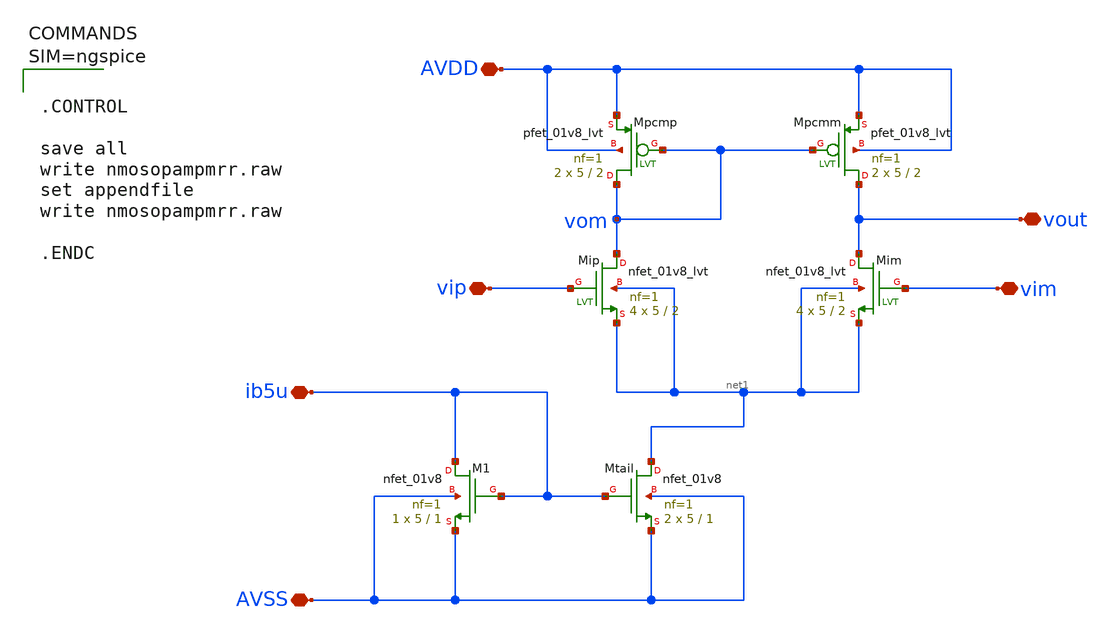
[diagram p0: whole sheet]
** sch_path: work/xschem/nmosopampmrr.sch
**.subckt nmosopampmrr ib5u vip vim AVDD AVSS vout
*.iopin ib5u
*.iopin vip
*.iopin vim
*.iopin AVDD
*.iopin AVSS
*.iopin vout
XMtail net1 ib5u AVSS AVSS sky130_fd_pr__nfet_01v8 L=1 W=5 nf=1 ad='int((1 + 1)/2) * 5 / 1 * 0.29' as='int((1 + 2)/2) * 5 / 1 * 0.29'
+ pd='2*int((1 + 1)/2) * (5 / 1 + 0.29)' ps='2*int((1 + 2)/2) * (5 / 1 + 0.29)' nrd='0.29 / 5 ' nrs='0.29 / 5 '
+ sa=0 sb=0 sd=0 mult=2 m=2
XM1 ib5u ib5u AVSS AVSS sky130_fd_pr__nfet_01v8 L=1 W=5 nf=1 ad='int((1 + 1)/2) * 5 / 1 * 0.29' as='int((1 + 2)/2) * 5 / 1 * 0.29'
+ pd='2*int((1 + 1)/2) * (5 / 1 + 0.29)' ps='2*int((1 + 2)/2) * (5 / 1 + 0.29)' nrd='0.29 / 5 ' nrs='0.29 / 5 '
+ sa=0 sb=0 sd=0 mult=1 m=1
XMip vom vip net1 net1 sky130_fd_pr__nfet_01v8_lvt L=2 W=5 nf=1 ad='int((1 + 1)/2) * 5 / 1 * 0.29' as='int((1 + 2)/2) * 5 / 1 * 0.29'
+ pd='2*int((1 + 1)/2) * (5 / 1 + 0.29)' ps='2*int((1 + 2)/2) * (5 / 1 + 0.29)' nrd='0.29 / 5 ' nrs='0.29 / 5 '
+ sa=0 sb=0 sd=0 mult=4 m=4
XMim vout vim net1 net1 sky130_fd_pr__nfet_01v8_lvt L=2 W=5 nf=1 ad='int((1 + 1)/2) * 5 / 1 * 0.29' as='int((1 + 2)/2) * 5 / 1 * 0.29'
+ pd='2*int((1 + 1)/2) * (5 / 1 + 0.29)' ps='2*int((1 + 2)/2) * (5 / 1 + 0.29)' nrd='0.29 / 5 ' nrs='0.29 / 5 '
+ sa=0 sb=0 sd=0 mult=4 m=4
XMpcmm vout vom AVDD AVDD sky130_fd_pr__pfet_01v8_lvt L=2 W=5 nf=1 ad='int((1 + 1)/2) * 5 / 1 * 0.29'
+ as='int((1 + 2)/2) * 5 / 1 * 0.29' pd='2*int((1 + 1)/2) * (5 / 1 + 0.29)' ps='2*int((1 + 2)/2) * (5 / 1 + 0.29)'
+ nrd='0.29 / 5 ' nrs='0.29 / 5 ' sa=0 sb=0 sd=0 mult=2 m=2
XMpcmp vom vom AVDD AVDD sky130_fd_pr__pfet_01v8_lvt L=2 W=5 nf=1 ad='int((1 + 1)/2) * 5 / 1 * 0.29'
+ as='int((1 + 2)/2) * 5 / 1 * 0.29' pd='2*int((1 + 1)/2) * (5 / 1 + 0.29)' ps='2*int((1 + 2)/2) * (5 / 1 + 0.29)'
+ nrd='0.29 / 5 ' nrs='0.29 / 5 ' sa=0 sb=0 sd=0 mult=2 m=2
**** begin user architecture code



.CONTROL

save all
write nmosopampmrr.raw
set appendfile
write nmosopampmrr.raw

.ENDC



**** end user architecture code
**.ends
.end
